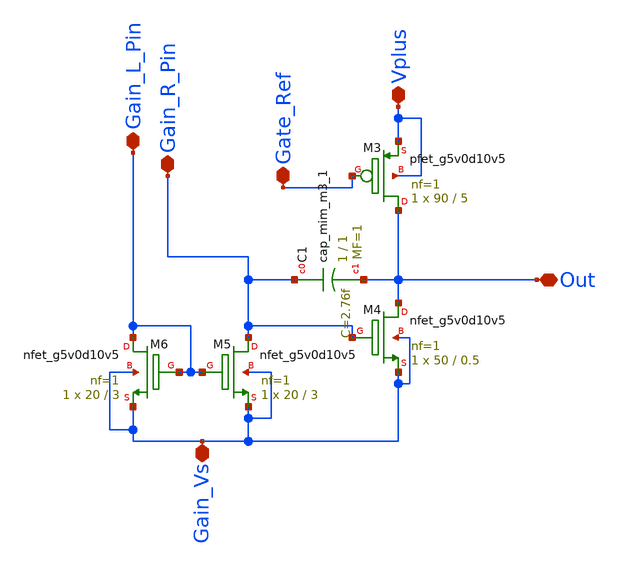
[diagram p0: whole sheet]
** sch_path: xschem/PrimalStructures/GainStage.sch
**.subckt GainStage Vplus Gain_L_Pin Gain_R_Pin Gate_Ref Out Gain_Vs
*.iopin Vplus
*.iopin Gain_L_Pin
*.iopin Gain_R_Pin
*.iopin Gate_Ref
*.iopin Out
*.iopin Gain_Vs
XM3 Out Gate_Ref Vplus Vplus sky130_fd_pr__pfet_g5v0d10v5 L=5 W=90 nf=1 ad='int((nf+1)/2) * W/nf * 0.29'
+ as='int((nf+2)/2) * W/nf * 0.29' pd='2*int((nf+1)/2) * (W/nf + 0.29)' ps='2*int((nf+2)/2) * (W/nf + 0.29)'
+ nrd='0.29 / W' nrs='0.29 / W' sa=0 sb=0 sd=0 mult=1 m=1
XM4 Out Gain_R_Pin Gain_Vs Gain_Vs sky130_fd_pr__nfet_g5v0d10v5 L=0.5 W=50 nf=1 ad='int((nf+1)/2) * W/nf * 0.29'
+ as='int((nf+2)/2) * W/nf * 0.29' pd='2*int((nf+1)/2) * (W/nf + 0.29)' ps='2*int((nf+2)/2) * (W/nf + 0.29)'
+ nrd='0.29 / W' nrs='0.29 / W' sa=0 sb=0 sd=0 mult=1 m=1
XM5 Gain_R_Pin Gain_L_Pin Gain_Vs Gain_Vs sky130_fd_pr__nfet_g5v0d10v5 L=3 W=20 nf=1 ad='int((nf+1)/2) * W/nf * 0.29'
+ as='int((nf+2)/2) * W/nf * 0.29' pd='2*int((nf+1)/2) * (W/nf + 0.29)' ps='2*int((nf+2)/2) * (W/nf + 0.29)'
+ nrd='0.29 / W' nrs='0.29 / W' sa=0 sb=0 sd=0 mult=1 m=1
XM6 Gain_L_Pin Gain_L_Pin Gain_Vs Gain_Vs sky130_fd_pr__nfet_g5v0d10v5 L=3 W=20 nf=1 ad='int((nf+1)/2) * W/nf * 0.29'
+ as='int((nf+2)/2) * W/nf * 0.29' pd='2*int((nf+1)/2) * (W/nf + 0.29)' ps='2*int((nf+2)/2) * (W/nf + 0.29)'
+ nrd='0.29 / W' nrs='0.29 / W' sa=0 sb=0 sd=0 mult=1 m=1
XC1 Gain_R_Pin Out sky130_fd_pr__cap_mim_m3_1 W=1 L=1 MF=1 m=1
**.ends
.end
